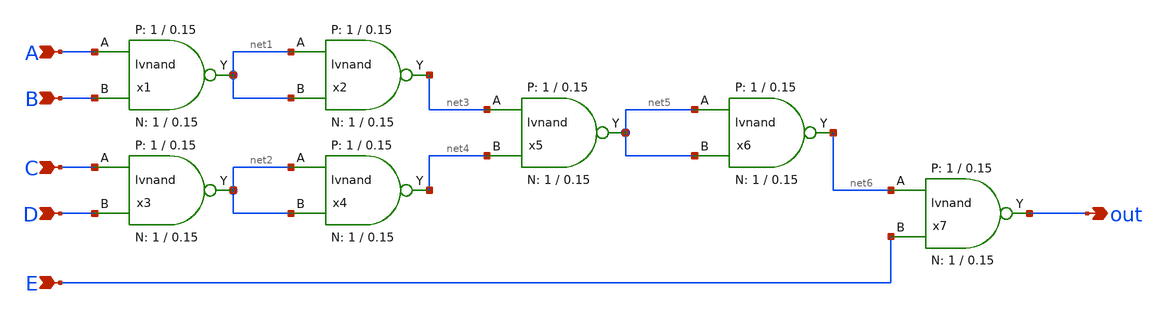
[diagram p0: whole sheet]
** sch_path: analog/schematics/5-nand.sch
* StefanSchippers/xschem_sky130/sky130_tests/lvnand.sch:
* Copyright 2021 Stefan Frederik Schippers
* Licensed under the Apache License, Version 2.0 (the "License");
**.subckt 5-nand A B C D E out
*.ipin A
*.ipin B
*.ipin C
*.ipin D
*.ipin E
*.opin out
x1 A B net1 VCC VSS lvnand WidthN=1 LenN=0.15 WidthP=1 LenP=0.15 m=1
x2 net1 net1 net3 VCC VSS lvnand WidthN=1 LenN=0.15 WidthP=1 LenP=0.15 m=1
x3 C D net2 VCC VSS lvnand WidthN=1 LenN=0.15 WidthP=1 LenP=0.15 m=1
x4 net2 net2 net4 VCC VSS lvnand WidthN=1 LenN=0.15 WidthP=1 LenP=0.15 m=1
x5 net3 net4 net5 VCC VSS lvnand WidthN=1 LenN=0.15 WidthP=1 LenP=0.15 m=1
x6 net5 net5 net6 VCC VSS lvnand WidthN=1 LenN=0.15 WidthP=1 LenP=0.15 m=1
x7 net6 E out VCC VSS lvnand WidthN=1 LenN=0.15 WidthP=1 LenP=0.15 m=1
**.ends

* expanding   symbol:  sky130_tests/lvnand.sym # of pins=3
** sym_path: sky130_tests/lvnand.sym
** sch_path: sky130_tests/lvnand.sch
.subckt lvnand A B Y VCCPIN VSSPIN  WidthN=1 LenN=0.15 WidthP=1 LenP=0.15
*.ipin A
*.ipin B
*.opin Y
XM1 Y B S VSSPIN sky130_fd_pr__nfet_01v8 L=LenN W=WidthN nf=1 ad='int((nf+1)/2) * W/nf * 0.29' as='int((nf+2)/2) * W/nf * 0.29'
+ pd='2*int((nf+1)/2) * (W/nf + 0.29)' ps='2*int((nf+2)/2) * (W/nf + 0.29)' nrd='0.29 / W' nrs='0.29 / W'
+ sa=0 sb=0 sd=0 mult=1 m=1
XM2 Y A VCCPIN VCCPIN sky130_fd_pr__pfet_01v8 L=LenP W=WidthP nf=1 ad='int((nf+1)/2) * W/nf * 0.29' as='int((nf+2)/2) * W/nf * 0.29'
+ pd='2*int((nf+1)/2) * (W/nf + 0.29)' ps='2*int((nf+2)/2) * (W/nf + 0.29)' nrd='0.29 / W' nrs='0.29 / W'
+ sa=0 sb=0 sd=0 mult=1 m=1
XM3 Y B VCCPIN VCCPIN sky130_fd_pr__pfet_01v8 L=LenP W=WidthP nf=1 ad='int((nf+1)/2) * W/nf * 0.29' as='int((nf+2)/2) * W/nf * 0.29'
+ pd='2*int((nf+1)/2) * (W/nf + 0.29)' ps='2*int((nf+2)/2) * (W/nf + 0.29)' nrd='0.29 / W' nrs='0.29 / W'
+ sa=0 sb=0 sd=0 mult=1 m=1
XM4 S A VSSPIN VSSPIN sky130_fd_pr__nfet_01v8 L=LenN W=WidthN nf=1 ad='int((nf+1)/2) * W/nf * 0.29' as='int((nf+2)/2) * W/nf * 0.29'
+ pd='2*int((nf+1)/2) * (W/nf + 0.29)' ps='2*int((nf+2)/2) * (W/nf + 0.29)' nrd='0.29 / W' nrs='0.29 / W'
+ sa=0 sb=0 sd=0 mult=1 m=1
.ends

.end
